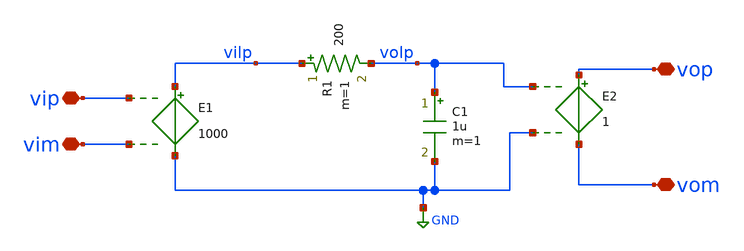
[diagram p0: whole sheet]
** sch_path: xschem/opa_mod1.sch
**.subckt opa_mod1 vop vom vip vim
*.iopin vop
*.iopin vom
*.iopin vip
*.iopin vim
E1 vilp GND vip vim 1000
R1 vilp volp 200 m=1
C1 volp GND 1u m=1
E2 vop vom volp GND 1
**.ends
.GLOBAL GND
.end
